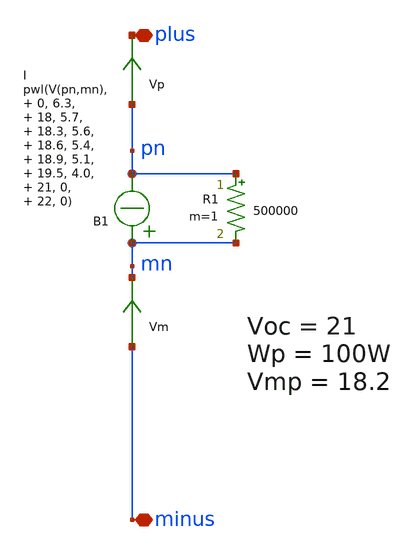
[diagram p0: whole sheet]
** sch_path: xschem_library/ngspice/pv_ngspice.sch
**.subckt pv_ngspice plus minus
*.iopin plus
*.iopin minus
Vm minus mn 0
.save i(vm)
Vp pn plus 0
.save i(vp)
B1 mn pn I = pwl(V(pn,mn), 0, 6.3, 18, 5.7, 18.3, 5.6, 18.6, 5.4, 18.9, 5.1, 19.5, 4.0, 21, 0, 22,
+ 0)
R1 pn mn 500000 m=1
**.ends
.end
